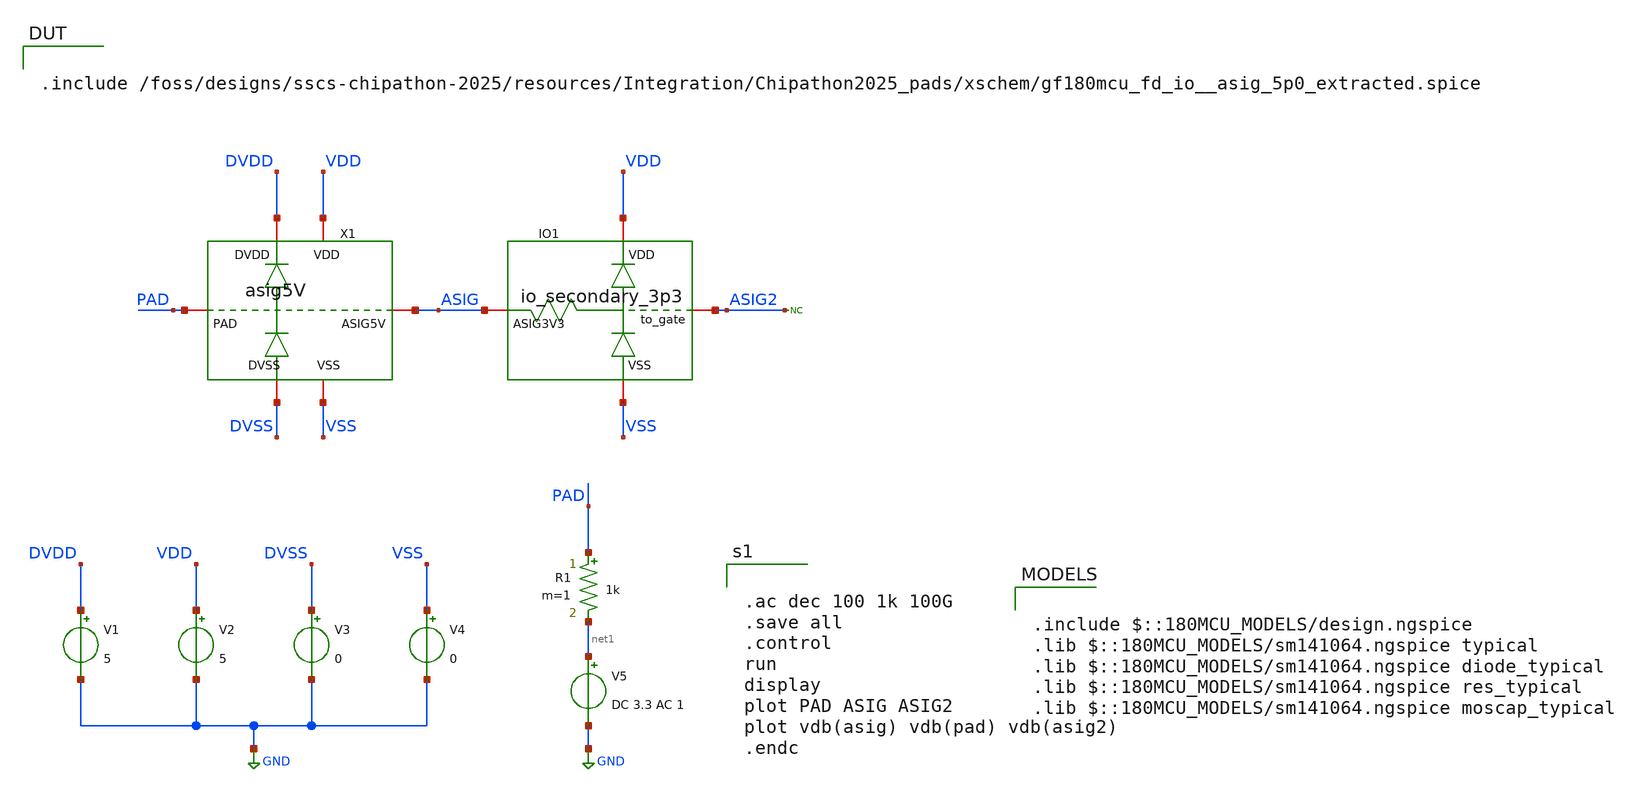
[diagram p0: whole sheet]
** sch_path: examples/pads_simulation/PAD_2ESD_tb.sch
**.subckt PAD_2ESD_tb
V1 DVDD GND 5
V2 VDD GND 5
V3 DVSS GND 0
V4 VSS GND 0
V5 net1 GND DC 3.3 AC 1
R1 PAD net1 1k m=1
X1 DVSS DVDD VSS VDD PAD ASIG gf180mcu_fd_io__asig_5p0_extracted
XIO1 VDD ASIG2 ASIG VSS io_secondary_3p3
* noconn ASIG2
**** begin user architecture code

.include /foss/designs/sscs-chipathon-2025/resources/Integration/Chipathon2025_pads/xschem/gf180mcu_fd_io__asig_5p0_extracted.spice


.include $::180MCU_MODELS/design.ngspice
.lib $::180MCU_MODELS/sm141064.ngspice typical
.lib $::180MCU_MODELS/sm141064.ngspice diode_typical
.lib $::180MCU_MODELS/sm141064.ngspice res_typical
.lib $::180MCU_MODELS/sm141064.ngspice moscap_typical



.ac dec 100 1k 100G
.save all
.control
run
display
plot PAD ASIG ASIG2
plot vdb(asig) vdb(pad) vdb(asig2)
.endc


**** end user architecture code
**.ends

* expanding   symbol:  xschem/symbols/io_secondary_3p3/io_secondary_3p3.sym # of pins=4
** sym_path: resources/Integration/Chipathon2025_pads/xschem/symbols/io_secondary_3p3/io_secondary_3p3.sym
** sch_path: resources/Integration/Chipathon2025_pads/xschem/symbols/io_secondary_3p3/io_secondary_3p3.sch
.subckt io_secondary_3p3 VDD to_gate ASIG3V3 VSS


*.iopin VSS
*.iopin VDD
*.iopin to_gate
*.iopin ASIG3V3
XR1 to_gate ASIG3V3 VDD ppolyf_u r_width=16e-6 r_length=4e-6 m=1
D2 VSS to_gate diode_nd2ps_03v3 area='10u * 10u ' pj='2*10u + 2*10u ' m=4
D1 to_gate VDD diode_pd2nw_03v3 area='10u * 10u ' pj='2*10u + 2*10u ' m=4
.ends

.GLOBAL GND
.end
